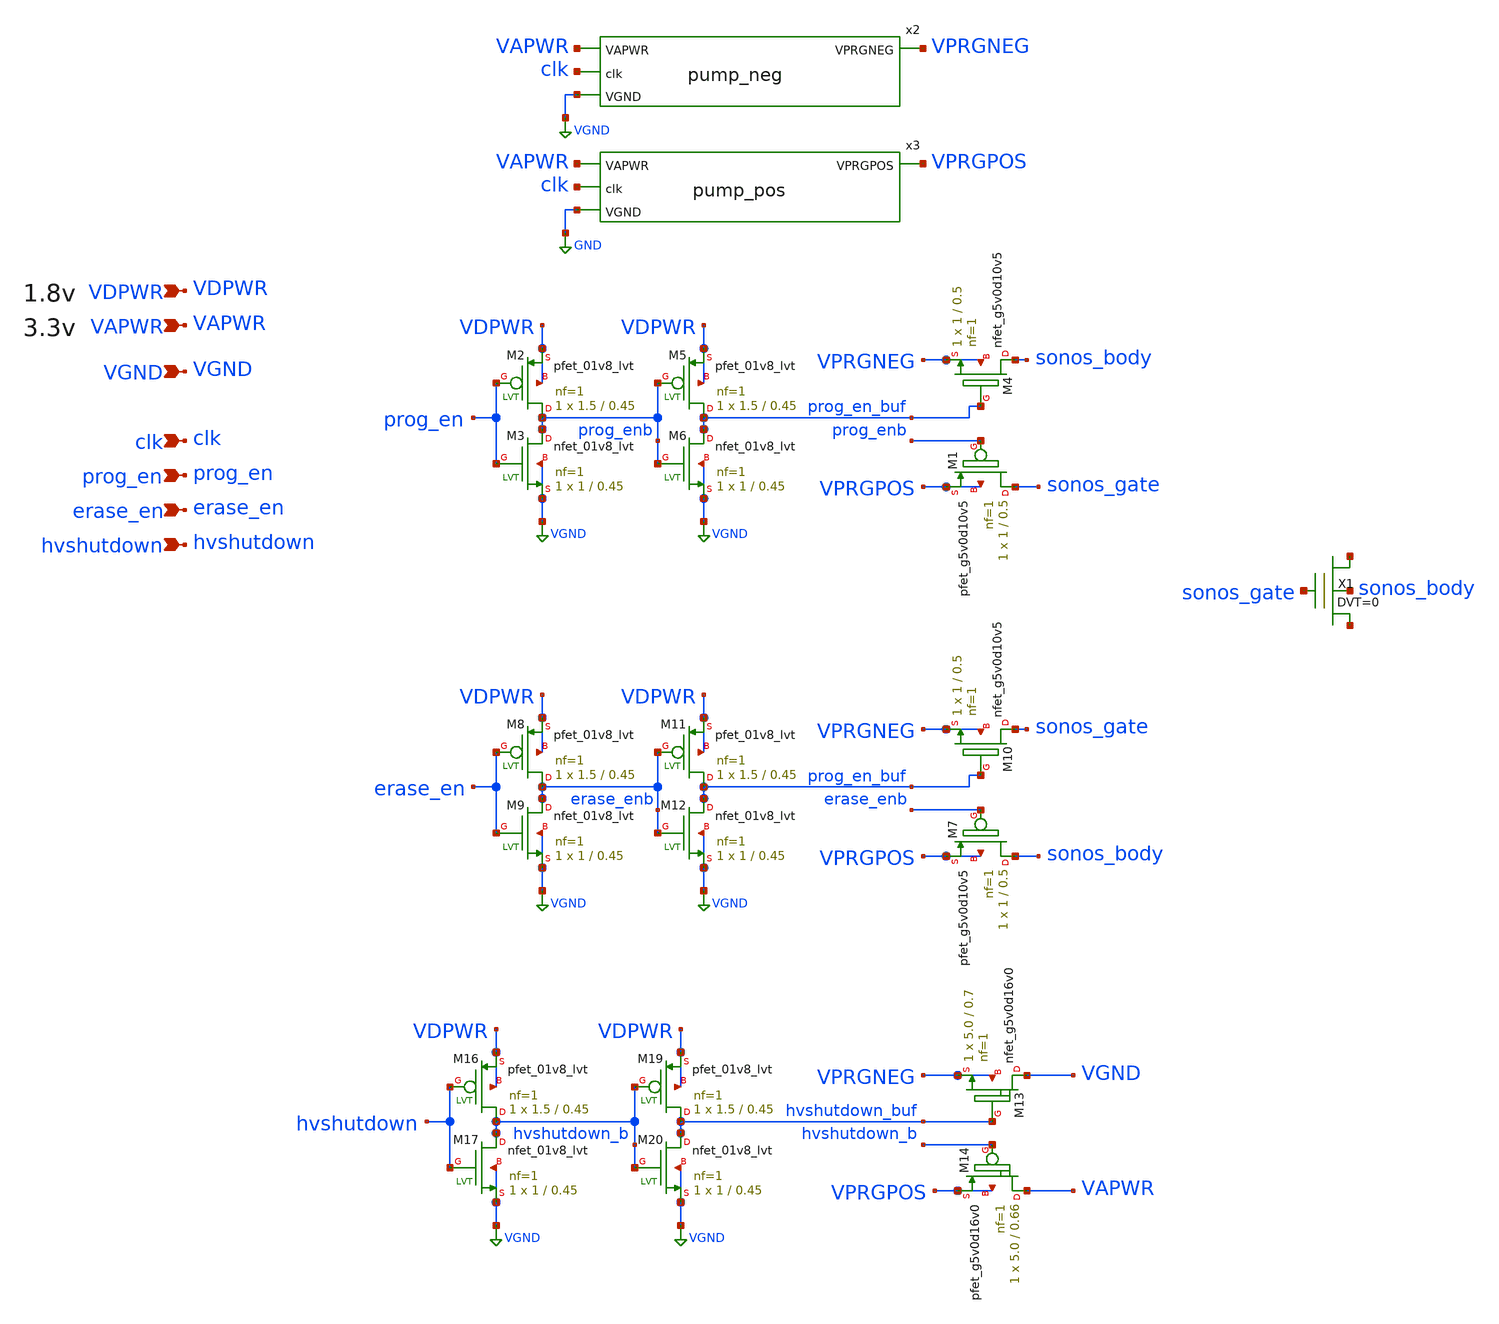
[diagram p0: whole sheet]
** sch_path: xschem/flash.sch
**.subckt flash VAPWR VGND clk prog_en erase_en VDPWR hvshutdown
*.ipin VAPWR
*.ipin VGND
*.ipin clk
*.ipin prog_en
*.ipin erase_en
*.ipin VDPWR
*.ipin hvshutdown
X1 net1 sonos_gate net2 sonos_body sky130_fd_pr__special_nfet_pass_flash w=0.45 l=0.15 m=1
x2 VAPWR VPRGNEG clk VGND pump_neg
x3 VAPWR VPRGPOS clk GND pump_pos
XM1 sonos_gate prog_enb VPRGPOS VPRGPOS sky130_fd_pr__pfet_g5v0d10v5 L=0.5 W=1 nf=1 ad='int((nf+1)/2) * W/nf * 0.29'
+ as='int((nf+2)/2) * W/nf * 0.29' pd='2*int((nf+1)/2) * (W/nf + 0.29)' ps='2*int((nf+2)/2) * (W/nf + 0.29)'
+ nrd='0.29 / W' nrs='0.29 / W' sa=0 sb=0 sd=0 mult=1 m=1
XM2 prog_enb prog_en VDPWR VDPWR sky130_fd_pr__pfet_01v8_lvt L=0.45 W=1.5 nf=1 ad='int((nf+1)/2) * W/nf * 0.29'
+ as='int((nf+2)/2) * W/nf * 0.29' pd='2*int((nf+1)/2) * (W/nf + 0.29)' ps='2*int((nf+2)/2) * (W/nf + 0.29)'
+ nrd='0.29 / W' nrs='0.29 / W' sa=0 sb=0 sd=0 mult=1 m=1
XM3 prog_enb prog_en VGND VGND sky130_fd_pr__nfet_01v8_lvt L=0.45 W=1 nf=1 ad='int((nf+1)/2) * W/nf * 0.29'
+ as='int((nf+2)/2) * W/nf * 0.29' pd='2*int((nf+1)/2) * (W/nf + 0.29)' ps='2*int((nf+2)/2) * (W/nf + 0.29)'
+ nrd='0.29 / W' nrs='0.29 / W' sa=0 sb=0 sd=0 mult=1 m=1
XM4 sonos_body prog_en_buf VPRGNEG VPRGNEG sky130_fd_pr__nfet_g5v0d10v5 L=0.5 W=1 nf=1 ad='int((nf+1)/2) * W/nf * 0.29'
+ as='int((nf+2)/2) * W/nf * 0.29' pd='2*int((nf+1)/2) * (W/nf + 0.29)' ps='2*int((nf+2)/2) * (W/nf + 0.29)'
+ nrd='0.29 / W' nrs='0.29 / W' sa=0 sb=0 sd=0 mult=1 m=1
XM5 prog_en_buf prog_enb VDPWR VDPWR sky130_fd_pr__pfet_01v8_lvt L=0.45 W=1.5 nf=1 ad='int((nf+1)/2) * W/nf * 0.29'
+ as='int((nf+2)/2) * W/nf * 0.29' pd='2*int((nf+1)/2) * (W/nf + 0.29)' ps='2*int((nf+2)/2) * (W/nf + 0.29)'
+ nrd='0.29 / W' nrs='0.29 / W' sa=0 sb=0 sd=0 mult=1 m=1
XM6 prog_en_buf prog_enb VGND VGND sky130_fd_pr__nfet_01v8_lvt L=0.45 W=1 nf=1 ad='int((nf+1)/2) * W/nf * 0.29'
+ as='int((nf+2)/2) * W/nf * 0.29' pd='2*int((nf+1)/2) * (W/nf + 0.29)' ps='2*int((nf+2)/2) * (W/nf + 0.29)'
+ nrd='0.29 / W' nrs='0.29 / W' sa=0 sb=0 sd=0 mult=1 m=1
XM7 sonos_body erase_enb VPRGPOS VPRGPOS sky130_fd_pr__pfet_g5v0d10v5 L=0.5 W=1 nf=1 ad='int((nf+1)/2) * W/nf * 0.29'
+ as='int((nf+2)/2) * W/nf * 0.29' pd='2*int((nf+1)/2) * (W/nf + 0.29)' ps='2*int((nf+2)/2) * (W/nf + 0.29)'
+ nrd='0.29 / W' nrs='0.29 / W' sa=0 sb=0 sd=0 mult=1 m=1
XM8 erase_enb erase_en VDPWR VDPWR sky130_fd_pr__pfet_01v8_lvt L=0.45 W=1.5 nf=1 ad='int((nf+1)/2) * W/nf * 0.29'
+ as='int((nf+2)/2) * W/nf * 0.29' pd='2*int((nf+1)/2) * (W/nf + 0.29)' ps='2*int((nf+2)/2) * (W/nf + 0.29)'
+ nrd='0.29 / W' nrs='0.29 / W' sa=0 sb=0 sd=0 mult=1 m=1
XM9 erase_enb erase_en VGND VGND sky130_fd_pr__nfet_01v8_lvt L=0.45 W=1 nf=1 ad='int((nf+1)/2) * W/nf * 0.29'
+ as='int((nf+2)/2) * W/nf * 0.29' pd='2*int((nf+1)/2) * (W/nf + 0.29)' ps='2*int((nf+2)/2) * (W/nf + 0.29)'
+ nrd='0.29 / W' nrs='0.29 / W' sa=0 sb=0 sd=0 mult=1 m=1
XM10 sonos_gate prog_en_buf VPRGNEG VPRGNEG sky130_fd_pr__nfet_g5v0d10v5 L=0.5 W=1 nf=1 ad='int((nf+1)/2) * W/nf * 0.29'
+ as='int((nf+2)/2) * W/nf * 0.29' pd='2*int((nf+1)/2) * (W/nf + 0.29)' ps='2*int((nf+2)/2) * (W/nf + 0.29)'
+ nrd='0.29 / W' nrs='0.29 / W' sa=0 sb=0 sd=0 mult=1 m=1
XM11 prog_en_buf erase_enb VDPWR VDPWR sky130_fd_pr__pfet_01v8_lvt L=0.45 W=1.5 nf=1 ad='int((nf+1)/2) * W/nf * 0.29'
+ as='int((nf+2)/2) * W/nf * 0.29' pd='2*int((nf+1)/2) * (W/nf + 0.29)' ps='2*int((nf+2)/2) * (W/nf + 0.29)'
+ nrd='0.29 / W' nrs='0.29 / W' sa=0 sb=0 sd=0 mult=1 m=1
XM12 prog_en_buf erase_enb VGND VGND sky130_fd_pr__nfet_01v8_lvt L=0.45 W=1 nf=1 ad='int((nf+1)/2) * W/nf * 0.29'
+ as='int((nf+2)/2) * W/nf * 0.29' pd='2*int((nf+1)/2) * (W/nf + 0.29)' ps='2*int((nf+2)/2) * (W/nf + 0.29)'
+ nrd='0.29 / W' nrs='0.29 / W' sa=0 sb=0 sd=0 mult=1 m=1
XM13 VGND hvshutdown_buf VPRGNEG VPRGNEG sky130_fd_pr__nfet_g5v0d16v0 L=0.7 W=5.0 nf=1 ad='int((nf+1)/2) * W/nf * 0.29'
+ as='int((nf+2)/2) * W/nf * 0.29' pd='2*int((nf+1)/2) * (W/nf + 0.29)' ps='2*int((nf+2)/2) * (W/nf + 0.29)'
+ nrd='0.29 / W' nrs='0.29 / W' sa=0 sb=0 sd=0 mult=1 m=1
XM14 VAPWR hvshutdown_b VPRGPOS VPRGPOS sky130_fd_pr__pfet_g5v0d16v0 L=0.66 W=5.0 nf=1 ad='int((nf+1)/2) * W/nf * 0.29'
+ as='int((nf+2)/2) * W/nf * 0.29' pd='2*int((nf+1)/2) * (W/nf + 0.29)' ps='2*int((nf+2)/2) * (W/nf + 0.29)'
+ nrd='0.29 / W' nrs='0.29 / W' sa=0 sb=0 sd=0 mult=1 m=1
XM16 hvshutdown_b hvshutdown VDPWR VDPWR sky130_fd_pr__pfet_01v8_lvt L=0.45 W=1.5 nf=1 ad='int((nf+1)/2) * W/nf * 0.29'
+ as='int((nf+2)/2) * W/nf * 0.29' pd='2*int((nf+1)/2) * (W/nf + 0.29)' ps='2*int((nf+2)/2) * (W/nf + 0.29)'
+ nrd='0.29 / W' nrs='0.29 / W' sa=0 sb=0 sd=0 mult=1 m=1
XM17 hvshutdown_b hvshutdown VGND VGND sky130_fd_pr__nfet_01v8_lvt L=0.45 W=1 nf=1 ad='int((nf+1)/2) * W/nf * 0.29'
+ as='int((nf+2)/2) * W/nf * 0.29' pd='2*int((nf+1)/2) * (W/nf + 0.29)' ps='2*int((nf+2)/2) * (W/nf + 0.29)'
+ nrd='0.29 / W' nrs='0.29 / W' sa=0 sb=0 sd=0 mult=1 m=1
XM19 hvshutdown_buf hvshutdown_b VDPWR VDPWR sky130_fd_pr__pfet_01v8_lvt L=0.45 W=1.5 nf=1 ad='int((nf+1)/2) * W/nf * 0.29'
+ as='int((nf+2)/2) * W/nf * 0.29' pd='2*int((nf+1)/2) * (W/nf + 0.29)' ps='2*int((nf+2)/2) * (W/nf + 0.29)'
+ nrd='0.29 / W' nrs='0.29 / W' sa=0 sb=0 sd=0 mult=1 m=1
XM20 hvshutdown_buf hvshutdown_b VGND VGND sky130_fd_pr__nfet_01v8_lvt L=0.45 W=1 nf=1 ad='int((nf+1)/2) * W/nf * 0.29'
+ as='int((nf+2)/2) * W/nf * 0.29' pd='2*int((nf+1)/2) * (W/nf + 0.29)' ps='2*int((nf+2)/2) * (W/nf + 0.29)'
+ nrd='0.29 / W' nrs='0.29 / W' sa=0 sb=0 sd=0 mult=1 m=1
**.ends
.GLOBAL VGND
.GLOBAL GND
.end
